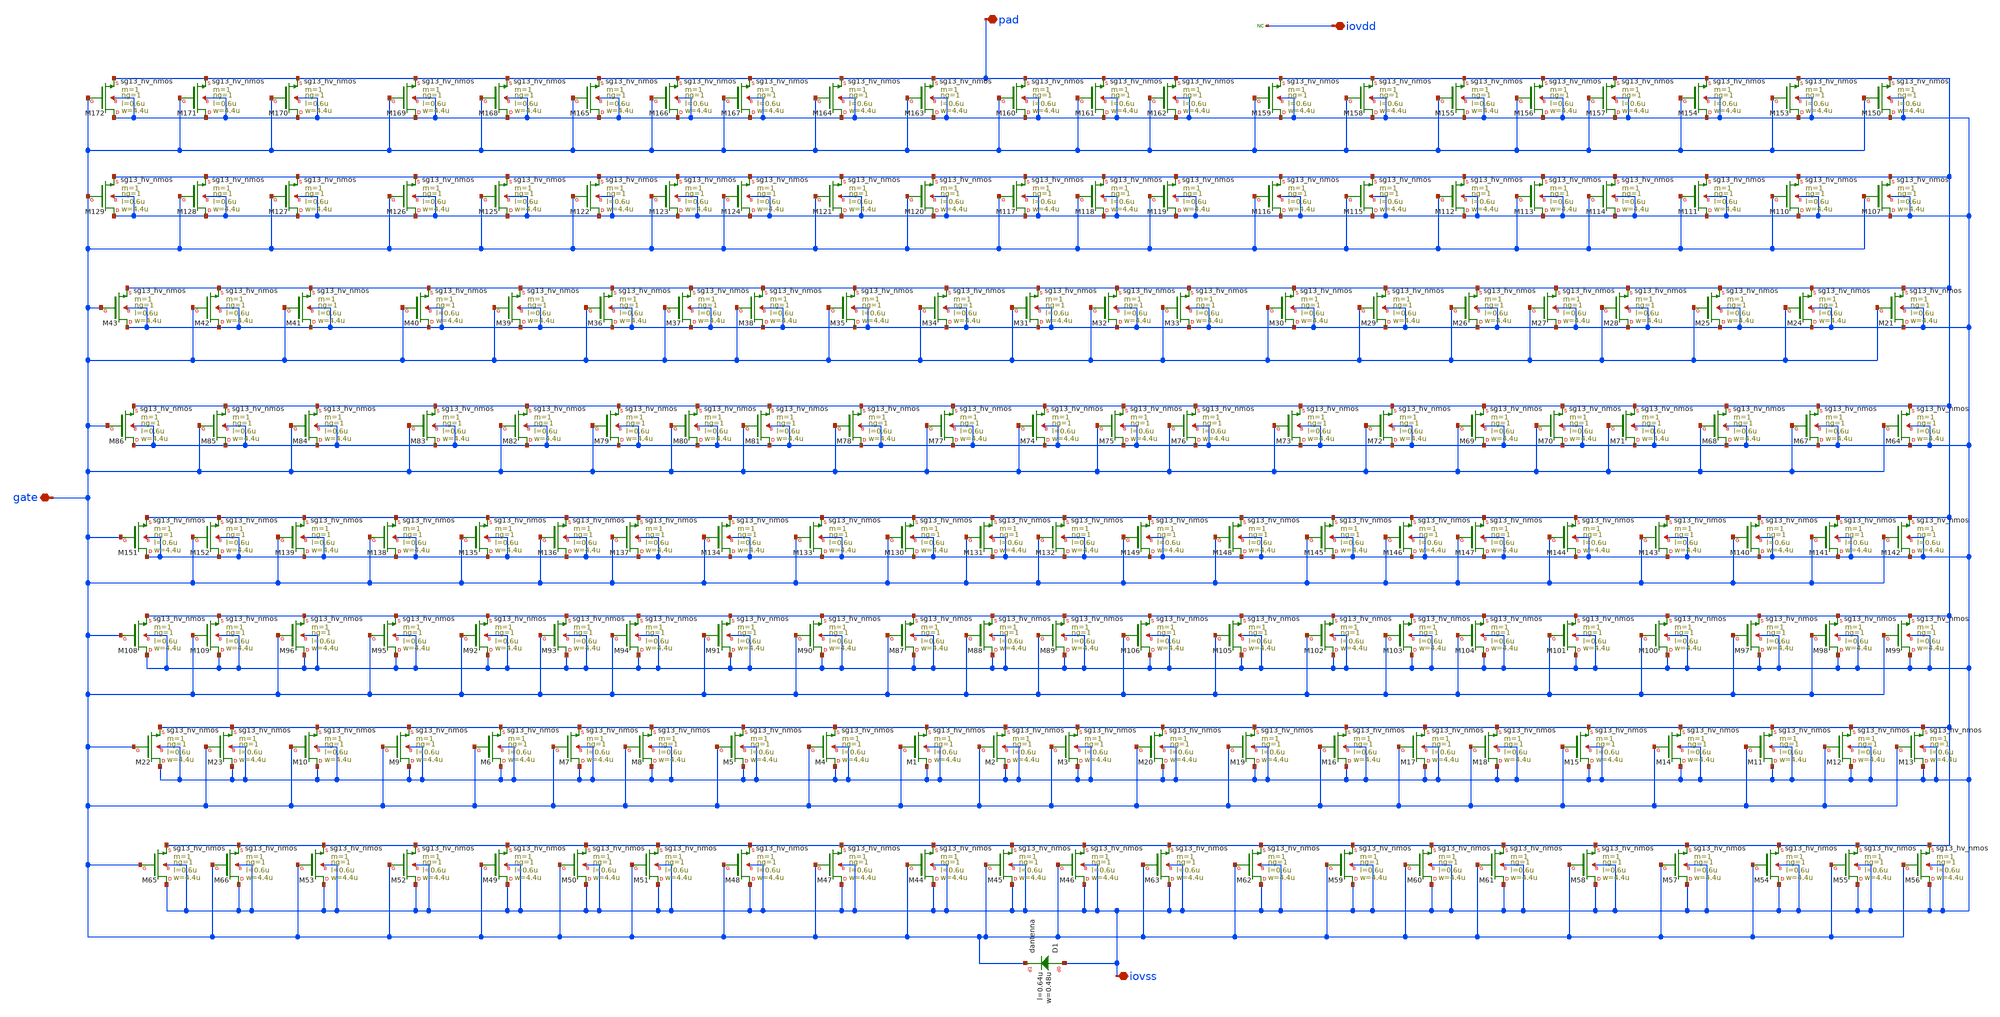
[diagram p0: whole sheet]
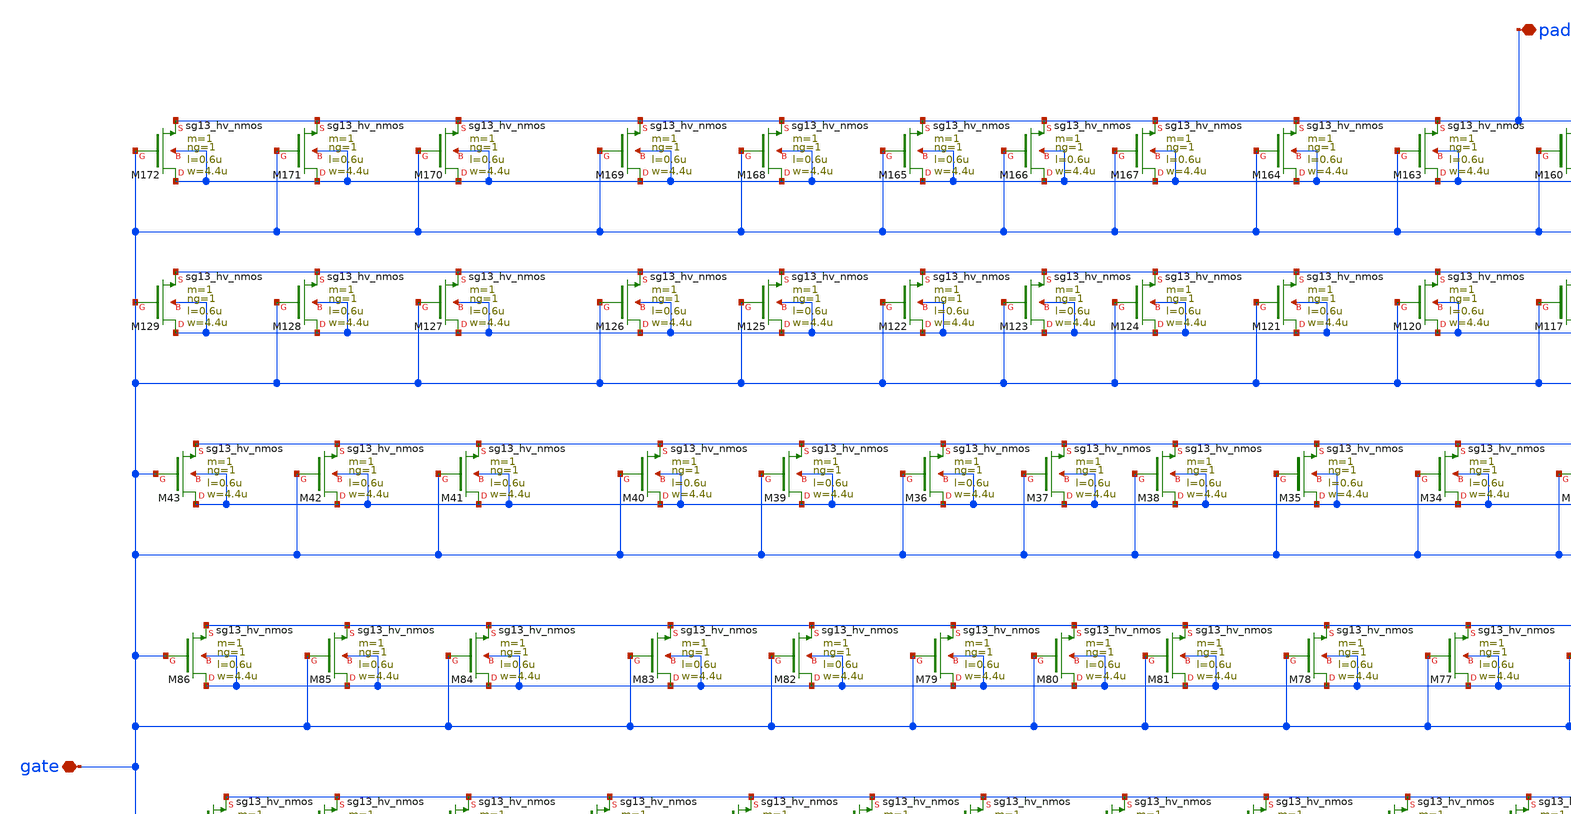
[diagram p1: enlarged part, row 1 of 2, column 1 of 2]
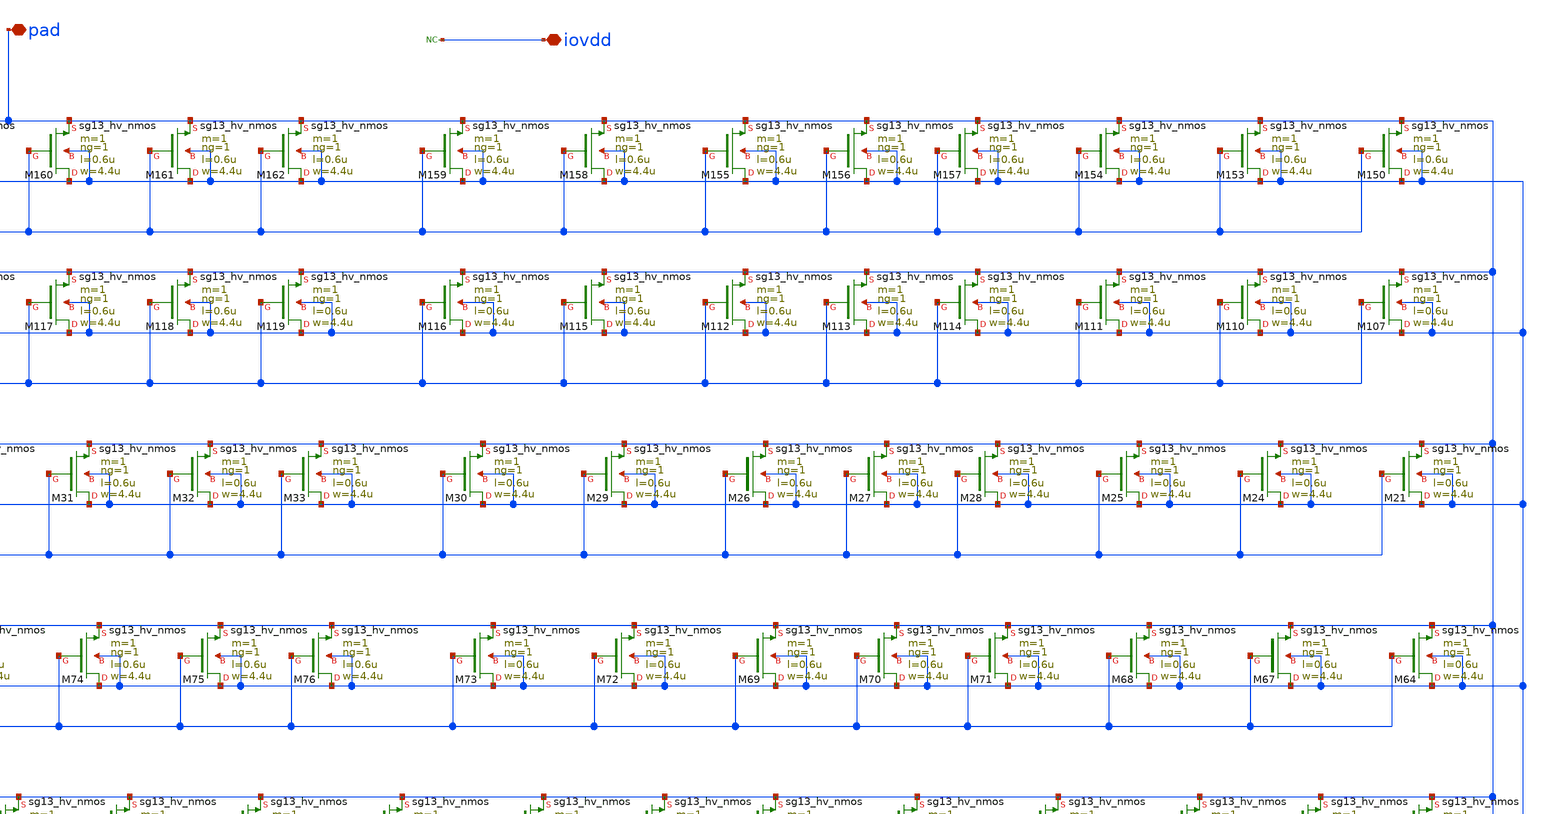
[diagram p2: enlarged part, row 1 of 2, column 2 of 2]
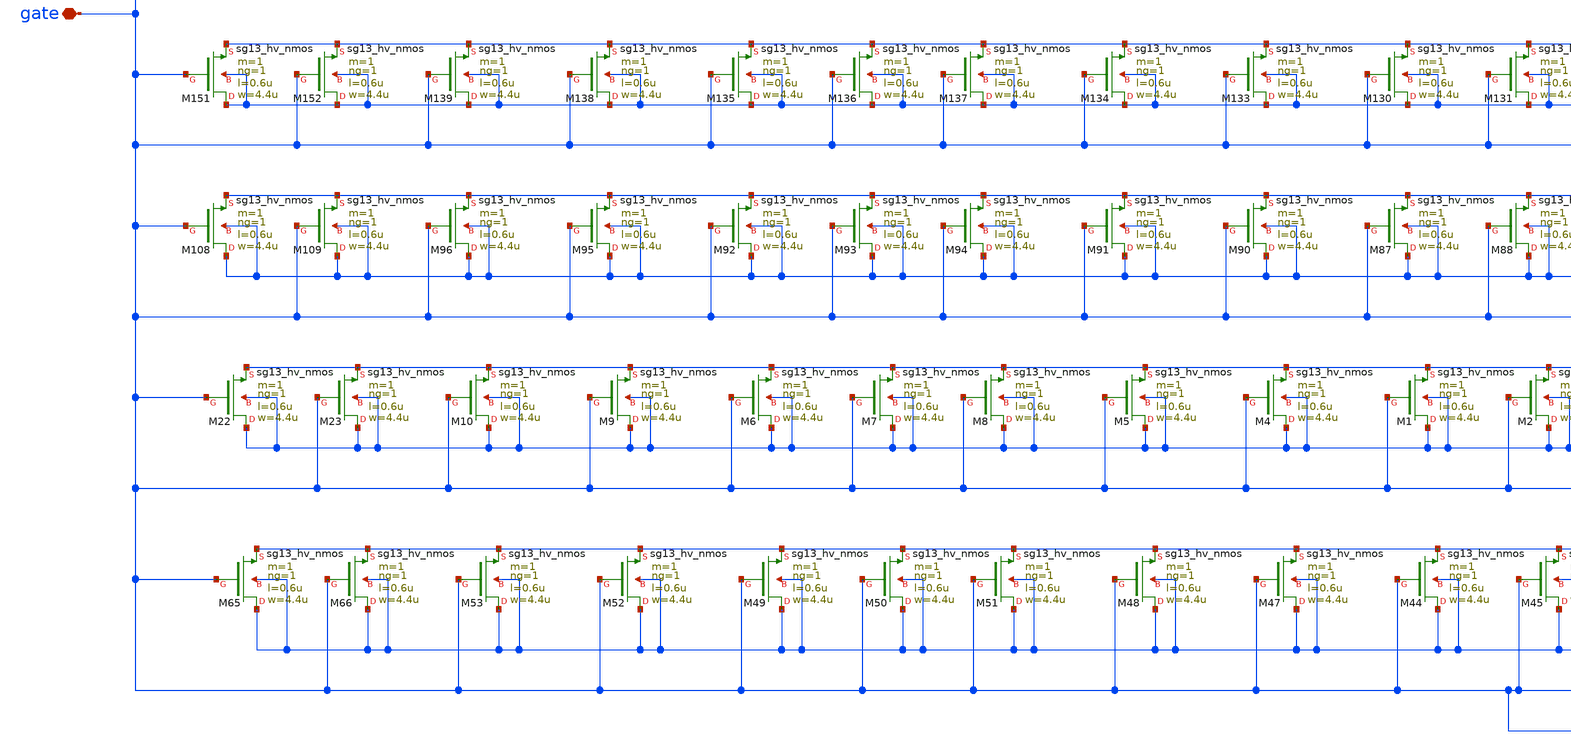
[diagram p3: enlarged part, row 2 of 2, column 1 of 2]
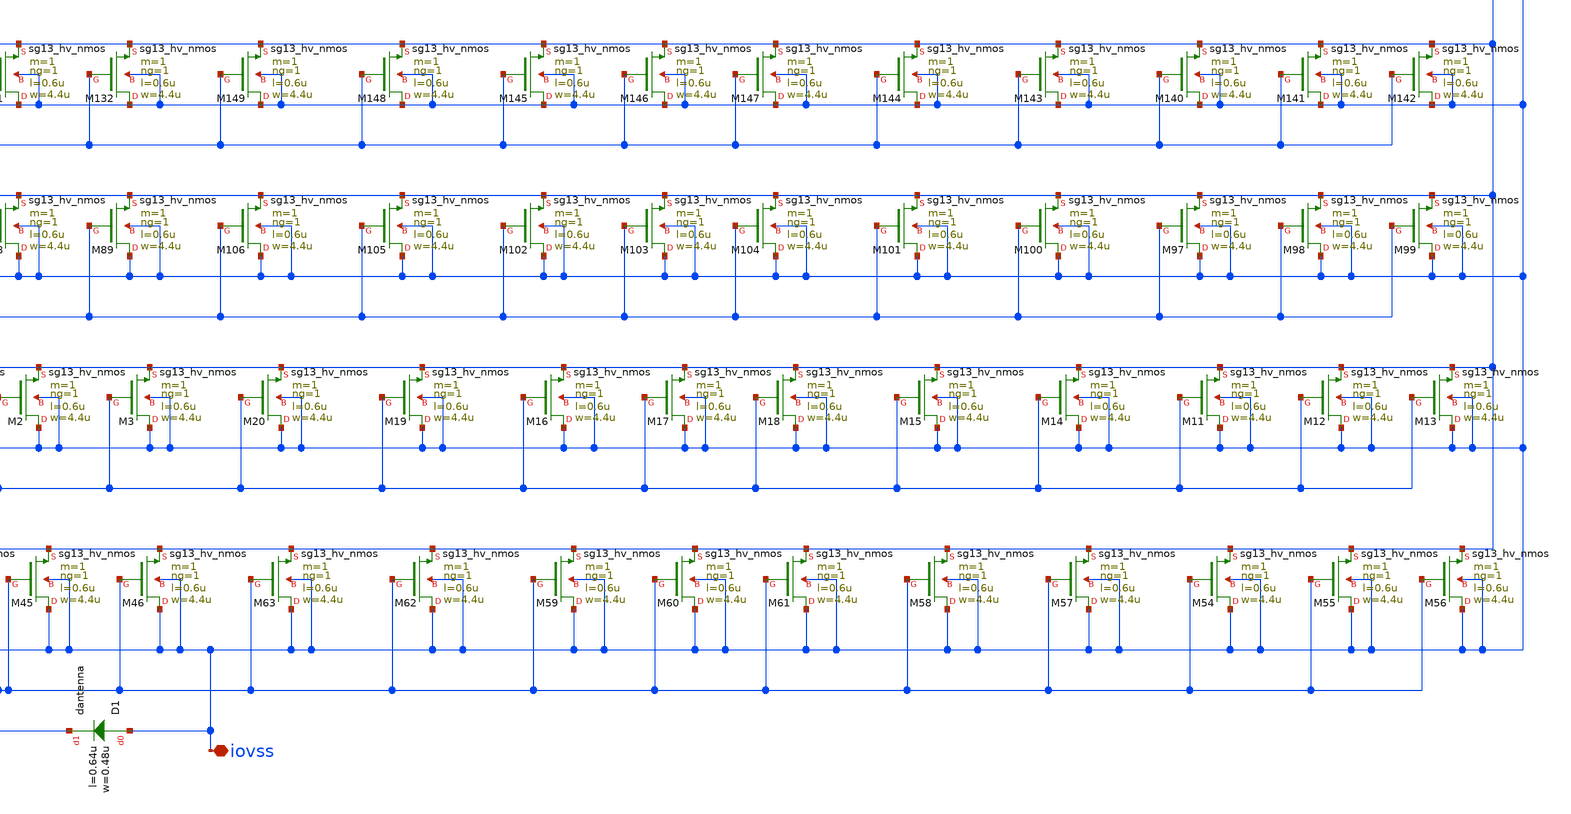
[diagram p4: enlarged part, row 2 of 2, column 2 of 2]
** sch_path: OTA_Telescopic_v3/Schematics_and_Symbols/IOCells/sg13g2_Clamp_N43N43D4R.sch
**.subckt sg13g2_Clamp_N43N43D4R pad iovss gate iovdd
*.iopin pad
*.iopin iovss
*.iopin gate
*.iopin iovdd
XM1 iovss gate pad iovss sg13_hv_nmos w=4.4u l=0.6u ng=1 m=1 mm_ok=1
XM2 iovss gate pad iovss sg13_hv_nmos w=4.4u l=0.6u ng=1 m=1 mm_ok=1
XM3 iovss gate pad iovss sg13_hv_nmos w=4.4u l=0.6u ng=1 m=1 mm_ok=1
XM4 iovss gate pad iovss sg13_hv_nmos w=4.4u l=0.6u ng=1 m=1 mm_ok=1
XM5 iovss gate pad iovss sg13_hv_nmos w=4.4u l=0.6u ng=1 m=1 mm_ok=1
XM6 iovss gate pad iovss sg13_hv_nmos w=4.4u l=0.6u ng=1 m=1 mm_ok=1
XM7 iovss gate pad iovss sg13_hv_nmos w=4.4u l=0.6u ng=1 m=1 mm_ok=1
XM8 iovss gate pad iovss sg13_hv_nmos w=4.4u l=0.6u ng=1 m=1 mm_ok=1
XM9 iovss gate pad iovss sg13_hv_nmos w=4.4u l=0.6u ng=1 m=1 mm_ok=1
XM10 iovss gate pad iovss sg13_hv_nmos w=4.4u l=0.6u ng=1 m=1 mm_ok=1
XM11 iovss gate pad iovss sg13_hv_nmos w=4.4u l=0.6u ng=1 m=1 mm_ok=1
XM12 iovss gate pad iovss sg13_hv_nmos w=4.4u l=0.6u ng=1 m=1 mm_ok=1
XM13 iovss gate pad iovss sg13_hv_nmos w=4.4u l=0.6u ng=1 m=1 mm_ok=1
XM14 iovss gate pad iovss sg13_hv_nmos w=4.4u l=0.6u ng=1 m=1 mm_ok=1
XM15 iovss gate pad iovss sg13_hv_nmos w=4.4u l=0.6u ng=1 m=1 mm_ok=1
XM16 iovss gate pad iovss sg13_hv_nmos w=4.4u l=0.6u ng=1 m=1 mm_ok=1
XM17 iovss gate pad iovss sg13_hv_nmos w=4.4u l=0.6u ng=1 m=1 mm_ok=1
XM18 iovss gate pad iovss sg13_hv_nmos w=4.4u l=0.6u ng=1 m=1 mm_ok=1
XM19 iovss gate pad iovss sg13_hv_nmos w=4.4u l=0.6u ng=1 m=1 mm_ok=1
XM20 iovss gate pad iovss sg13_hv_nmos w=4.4u l=0.6u ng=1 m=1 mm_ok=1
XM21 iovss gate pad iovss sg13_hv_nmos w=4.4u l=0.6u ng=1 m=1 mm_ok=1
XM22 iovss gate pad iovss sg13_hv_nmos w=4.4u l=0.6u ng=1 m=1 mm_ok=1
XM23 iovss gate pad iovss sg13_hv_nmos w=4.4u l=0.6u ng=1 m=1 mm_ok=1
XM24 iovss gate pad iovss sg13_hv_nmos w=4.4u l=0.6u ng=1 m=1 mm_ok=1
XM25 iovss gate pad iovss sg13_hv_nmos w=4.4u l=0.6u ng=1 m=1 mm_ok=1
XM26 iovss gate pad iovss sg13_hv_nmos w=4.4u l=0.6u ng=1 m=1 mm_ok=1
XM27 iovss gate pad iovss sg13_hv_nmos w=4.4u l=0.6u ng=1 m=1 mm_ok=1
XM28 iovss gate pad iovss sg13_hv_nmos w=4.4u l=0.6u ng=1 m=1 mm_ok=1
XM29 iovss gate pad iovss sg13_hv_nmos w=4.4u l=0.6u ng=1 m=1 mm_ok=1
XM30 iovss gate pad iovss sg13_hv_nmos w=4.4u l=0.6u ng=1 m=1 mm_ok=1
XM31 iovss gate pad iovss sg13_hv_nmos w=4.4u l=0.6u ng=1 m=1 mm_ok=1
XM32 iovss gate pad iovss sg13_hv_nmos w=4.4u l=0.6u ng=1 m=1 mm_ok=1
XM33 iovss gate pad iovss sg13_hv_nmos w=4.4u l=0.6u ng=1 m=1 mm_ok=1
XM34 iovss gate pad iovss sg13_hv_nmos w=4.4u l=0.6u ng=1 m=1 mm_ok=1
XM35 iovss gate pad iovss sg13_hv_nmos w=4.4u l=0.6u ng=1 m=1 mm_ok=1
XM36 iovss gate pad iovss sg13_hv_nmos w=4.4u l=0.6u ng=1 m=1 mm_ok=1
XM37 iovss gate pad iovss sg13_hv_nmos w=4.4u l=0.6u ng=1 m=1 mm_ok=1
XM38 iovss gate pad iovss sg13_hv_nmos w=4.4u l=0.6u ng=1 m=1 mm_ok=1
XM39 iovss gate pad iovss sg13_hv_nmos w=4.4u l=0.6u ng=1 m=1 mm_ok=1
XM40 iovss gate pad iovss sg13_hv_nmos w=4.4u l=0.6u ng=1 m=1 mm_ok=1
XM41 iovss gate pad iovss sg13_hv_nmos w=4.4u l=0.6u ng=1 m=1 mm_ok=1
XM42 iovss gate pad iovss sg13_hv_nmos w=4.4u l=0.6u ng=1 m=1 mm_ok=1
XM43 iovss gate pad iovss sg13_hv_nmos w=4.4u l=0.6u ng=1 m=1 mm_ok=1
XM44 iovss gate pad iovss sg13_hv_nmos w=4.4u l=0.6u ng=1 m=1 mm_ok=1
XM45 iovss gate pad iovss sg13_hv_nmos w=4.4u l=0.6u ng=1 m=1 mm_ok=1
XM46 iovss gate pad iovss sg13_hv_nmos w=4.4u l=0.6u ng=1 m=1 mm_ok=1
XM47 iovss gate pad iovss sg13_hv_nmos w=4.4u l=0.6u ng=1 m=1 mm_ok=1
XM48 iovss gate pad iovss sg13_hv_nmos w=4.4u l=0.6u ng=1 m=1 mm_ok=1
XM49 iovss gate pad iovss sg13_hv_nmos w=4.4u l=0.6u ng=1 m=1 mm_ok=1
XM50 iovss gate pad iovss sg13_hv_nmos w=4.4u l=0.6u ng=1 m=1 mm_ok=1
XM51 iovss gate pad iovss sg13_hv_nmos w=4.4u l=0.6u ng=1 m=1 mm_ok=1
XM52 iovss gate pad iovss sg13_hv_nmos w=4.4u l=0.6u ng=1 m=1 mm_ok=1
XM53 iovss gate pad iovss sg13_hv_nmos w=4.4u l=0.6u ng=1 m=1 mm_ok=1
XM54 iovss gate pad iovss sg13_hv_nmos w=4.4u l=0.6u ng=1 m=1 mm_ok=1
XM55 iovss gate pad iovss sg13_hv_nmos w=4.4u l=0.6u ng=1 m=1 mm_ok=1
XM56 iovss gate pad iovss sg13_hv_nmos w=4.4u l=0.6u ng=1 m=1 mm_ok=1
XM57 iovss gate pad iovss sg13_hv_nmos w=4.4u l=0.6u ng=1 m=1 mm_ok=1
XM58 iovss gate pad iovss sg13_hv_nmos w=4.4u l=0.6u ng=1 m=1 mm_ok=1
XM59 iovss gate pad iovss sg13_hv_nmos w=4.4u l=0.6u ng=1 m=1 mm_ok=1
XM60 iovss gate pad iovss sg13_hv_nmos w=4.4u l=0.6u ng=1 m=1 mm_ok=1
XM61 iovss gate pad iovss sg13_hv_nmos w=4.4u l=0.6u ng=1 m=1 mm_ok=1
XM62 iovss gate pad iovss sg13_hv_nmos w=4.4u l=0.6u ng=1 m=1 mm_ok=1
XM63 iovss gate pad iovss sg13_hv_nmos w=4.4u l=0.6u ng=1 m=1 mm_ok=1
XM64 iovss gate pad iovss sg13_hv_nmos w=4.4u l=0.6u ng=1 m=1 mm_ok=1
XM65 iovss gate pad iovss sg13_hv_nmos w=4.4u l=0.6u ng=1 m=1 mm_ok=1
XM66 iovss gate pad iovss sg13_hv_nmos w=4.4u l=0.6u ng=1 m=1 mm_ok=1
XM67 iovss gate pad iovss sg13_hv_nmos w=4.4u l=0.6u ng=1 m=1 mm_ok=1
XM68 iovss gate pad iovss sg13_hv_nmos w=4.4u l=0.6u ng=1 m=1 mm_ok=1
XM69 iovss gate pad iovss sg13_hv_nmos w=4.4u l=0.6u ng=1 m=1 mm_ok=1
XM70 iovss gate pad iovss sg13_hv_nmos w=4.4u l=0.6u ng=1 m=1 mm_ok=1
XM71 iovss gate pad iovss sg13_hv_nmos w=4.4u l=0.6u ng=1 m=1 mm_ok=1
XM72 iovss gate pad iovss sg13_hv_nmos w=4.4u l=0.6u ng=1 m=1 mm_ok=1
XM73 iovss gate pad iovss sg13_hv_nmos w=4.4u l=0.6u ng=1 m=1 mm_ok=1
XM74 iovss gate pad iovss sg13_hv_nmos w=4.4u l=0.6u ng=1 m=1 mm_ok=1
XM75 iovss gate pad iovss sg13_hv_nmos w=4.4u l=0.6u ng=1 m=1 mm_ok=1
XM76 iovss gate pad iovss sg13_hv_nmos w=4.4u l=0.6u ng=1 m=1 mm_ok=1
XM77 iovss gate pad iovss sg13_hv_nmos w=4.4u l=0.6u ng=1 m=1 mm_ok=1
XM78 iovss gate pad iovss sg13_hv_nmos w=4.4u l=0.6u ng=1 m=1 mm_ok=1
XM79 iovss gate pad iovss sg13_hv_nmos w=4.4u l=0.6u ng=1 m=1 mm_ok=1
XM80 iovss gate pad iovss sg13_hv_nmos w=4.4u l=0.6u ng=1 m=1 mm_ok=1
XM81 iovss gate pad iovss sg13_hv_nmos w=4.4u l=0.6u ng=1 m=1 mm_ok=1
XM82 iovss gate pad iovss sg13_hv_nmos w=4.4u l=0.6u ng=1 m=1 mm_ok=1
XM83 iovss gate pad iovss sg13_hv_nmos w=4.4u l=0.6u ng=1 m=1 mm_ok=1
XM84 iovss gate pad iovss sg13_hv_nmos w=4.4u l=0.6u ng=1 m=1 mm_ok=1
XM85 iovss gate pad iovss sg13_hv_nmos w=4.4u l=0.6u ng=1 m=1 mm_ok=1
XM86 iovss gate pad iovss sg13_hv_nmos w=4.4u l=0.6u ng=1 m=1 mm_ok=1
XM87 iovss gate pad iovss sg13_hv_nmos w=4.4u l=0.6u ng=1 m=1 mm_ok=1
XM88 iovss gate pad iovss sg13_hv_nmos w=4.4u l=0.6u ng=1 m=1 mm_ok=1
XM89 iovss gate pad iovss sg13_hv_nmos w=4.4u l=0.6u ng=1 m=1 mm_ok=1
XM90 iovss gate pad iovss sg13_hv_nmos w=4.4u l=0.6u ng=1 m=1 mm_ok=1
XM91 iovss gate pad iovss sg13_hv_nmos w=4.4u l=0.6u ng=1 m=1 mm_ok=1
XM92 iovss gate pad iovss sg13_hv_nmos w=4.4u l=0.6u ng=1 m=1 mm_ok=1
XM93 iovss gate pad iovss sg13_hv_nmos w=4.4u l=0.6u ng=1 m=1 mm_ok=1
XM94 iovss gate pad iovss sg13_hv_nmos w=4.4u l=0.6u ng=1 m=1 mm_ok=1
XM95 iovss gate pad iovss sg13_hv_nmos w=4.4u l=0.6u ng=1 m=1 mm_ok=1
XM96 iovss gate pad iovss sg13_hv_nmos w=4.4u l=0.6u ng=1 m=1 mm_ok=1
XM97 iovss gate pad iovss sg13_hv_nmos w=4.4u l=0.6u ng=1 m=1 mm_ok=1
XM98 iovss gate pad iovss sg13_hv_nmos w=4.4u l=0.6u ng=1 m=1 mm_ok=1
XM99 iovss gate pad iovss sg13_hv_nmos w=4.4u l=0.6u ng=1 m=1 mm_ok=1
XM100 iovss gate pad iovss sg13_hv_nmos w=4.4u l=0.6u ng=1 m=1 mm_ok=1
XM101 iovss gate pad iovss sg13_hv_nmos w=4.4u l=0.6u ng=1 m=1 mm_ok=1
XM102 iovss gate pad iovss sg13_hv_nmos w=4.4u l=0.6u ng=1 m=1 mm_ok=1
XM103 iovss gate pad iovss sg13_hv_nmos w=4.4u l=0.6u ng=1 m=1 mm_ok=1
XM104 iovss gate pad iovss sg13_hv_nmos w=4.4u l=0.6u ng=1 m=1 mm_ok=1
XM105 iovss gate pad iovss sg13_hv_nmos w=4.4u l=0.6u ng=1 m=1 mm_ok=1
XM106 iovss gate pad iovss sg13_hv_nmos w=4.4u l=0.6u ng=1 m=1 mm_ok=1
XM107 iovss gate pad iovss sg13_hv_nmos w=4.4u l=0.6u ng=1 m=1 mm_ok=1
XM108 iovss gate pad iovss sg13_hv_nmos w=4.4u l=0.6u ng=1 m=1 mm_ok=1
XM109 iovss gate pad iovss sg13_hv_nmos w=4.4u l=0.6u ng=1 m=1 mm_ok=1
XM110 iovss gate pad iovss sg13_hv_nmos w=4.4u l=0.6u ng=1 m=1 mm_ok=1
XM111 iovss gate pad iovss sg13_hv_nmos w=4.4u l=0.6u ng=1 m=1 mm_ok=1
XM112 iovss gate pad iovss sg13_hv_nmos w=4.4u l=0.6u ng=1 m=1 mm_ok=1
XM113 iovss gate pad iovss sg13_hv_nmos w=4.4u l=0.6u ng=1 m=1 mm_ok=1
XM114 iovss gate pad iovss sg13_hv_nmos w=4.4u l=0.6u ng=1 m=1 mm_ok=1
XM115 iovss gate pad iovss sg13_hv_nmos w=4.4u l=0.6u ng=1 m=1 mm_ok=1
XM116 iovss gate pad iovss sg13_hv_nmos w=4.4u l=0.6u ng=1 m=1 mm_ok=1
XM117 iovss gate pad iovss sg13_hv_nmos w=4.4u l=0.6u ng=1 m=1 mm_ok=1
XM118 iovss gate pad iovss sg13_hv_nmos w=4.4u l=0.6u ng=1 m=1 mm_ok=1
XM119 iovss gate pad iovss sg13_hv_nmos w=4.4u l=0.6u ng=1 m=1 mm_ok=1
XM120 iovss gate pad iovss sg13_hv_nmos w=4.4u l=0.6u ng=1 m=1 mm_ok=1
XM121 iovss gate pad iovss sg13_hv_nmos w=4.4u l=0.6u ng=1 m=1 mm_ok=1
XM122 iovss gate pad iovss sg13_hv_nmos w=4.4u l=0.6u ng=1 m=1 mm_ok=1
XM123 iovss gate pad iovss sg13_hv_nmos w=4.4u l=0.6u ng=1 m=1 mm_ok=1
XM124 iovss gate pad iovss sg13_hv_nmos w=4.4u l=0.6u ng=1 m=1 mm_ok=1
XM125 iovss gate pad iovss sg13_hv_nmos w=4.4u l=0.6u ng=1 m=1 mm_ok=1
XM126 iovss gate pad iovss sg13_hv_nmos w=4.4u l=0.6u ng=1 m=1 mm_ok=1
XM127 iovss gate pad iovss sg13_hv_nmos w=4.4u l=0.6u ng=1 m=1 mm_ok=1
XM128 iovss gate pad iovss sg13_hv_nmos w=4.4u l=0.6u ng=1 m=1 mm_ok=1
XM129 iovss gate pad iovss sg13_hv_nmos w=4.4u l=0.6u ng=1 m=1 mm_ok=1
XM130 iovss gate pad iovss sg13_hv_nmos w=4.4u l=0.6u ng=1 m=1 mm_ok=1
XM131 iovss gate pad iovss sg13_hv_nmos w=4.4u l=0.6u ng=1 m=1 mm_ok=1
XM132 iovss gate pad iovss sg13_hv_nmos w=4.4u l=0.6u ng=1 m=1 mm_ok=1
XM133 iovss gate pad iovss sg13_hv_nmos w=4.4u l=0.6u ng=1 m=1 mm_ok=1
XM134 iovss gate pad iovss sg13_hv_nmos w=4.4u l=0.6u ng=1 m=1 mm_ok=1
XM135 iovss gate pad iovss sg13_hv_nmos w=4.4u l=0.6u ng=1 m=1 mm_ok=1
XM136 iovss gate pad iovss sg13_hv_nmos w=4.4u l=0.6u ng=1 m=1 mm_ok=1
XM137 iovss gate pad iovss sg13_hv_nmos w=4.4u l=0.6u ng=1 m=1 mm_ok=1
XM138 iovss gate pad iovss sg13_hv_nmos w=4.4u l=0.6u ng=1 m=1 mm_ok=1
XM139 iovss gate pad iovss sg13_hv_nmos w=4.4u l=0.6u ng=1 m=1 mm_ok=1
XM140 iovss gate pad iovss sg13_hv_nmos w=4.4u l=0.6u ng=1 m=1 mm_ok=1
XM141 iovss gate pad iovss sg13_hv_nmos w=4.4u l=0.6u ng=1 m=1 mm_ok=1
XM142 iovss gate pad iovss sg13_hv_nmos w=4.4u l=0.6u ng=1 m=1 mm_ok=1
XM143 iovss gate pad iovss sg13_hv_nmos w=4.4u l=0.6u ng=1 m=1 mm_ok=1
XM144 iovss gate pad iovss sg13_hv_nmos w=4.4u l=0.6u ng=1 m=1 mm_ok=1
XM145 iovss gate pad iovss sg13_hv_nmos w=4.4u l=0.6u ng=1 m=1 mm_ok=1
XM146 iovss gate pad iovss sg13_hv_nmos w=4.4u l=0.6u ng=1 m=1 mm_ok=1
XM147 iovss gate pad iovss sg13_hv_nmos w=4.4u l=0.6u ng=1 m=1 mm_ok=1
XM148 iovss gate pad iovss sg13_hv_nmos w=4.4u l=0.6u ng=1 m=1 mm_ok=1
XM149 iovss gate pad iovss sg13_hv_nmos w=4.4u l=0.6u ng=1 m=1 mm_ok=1
XM150 iovss gate pad iovss sg13_hv_nmos w=4.4u l=0.6u ng=1 m=1 mm_ok=1
XM151 iovss gate pad iovss sg13_hv_nmos w=4.4u l=0.6u ng=1 m=1 mm_ok=1
XM152 iovss gate pad iovss sg13_hv_nmos w=4.4u l=0.6u ng=1 m=1 mm_ok=1
XM153 iovss gate pad iovss sg13_hv_nmos w=4.4u l=0.6u ng=1 m=1 mm_ok=1
XM154 iovss gate pad iovss sg13_hv_nmos w=4.4u l=0.6u ng=1 m=1 mm_ok=1
XM155 iovss gate pad iovss sg13_hv_nmos w=4.4u l=0.6u ng=1 m=1 mm_ok=1
XM156 iovss gate pad iovss sg13_hv_nmos w=4.4u l=0.6u ng=1 m=1 mm_ok=1
XM157 iovss gate pad iovss sg13_hv_nmos w=4.4u l=0.6u ng=1 m=1 mm_ok=1
XM158 iovss gate pad iovss sg13_hv_nmos w=4.4u l=0.6u ng=1 m=1 mm_ok=1
XM159 iovss gate pad iovss sg13_hv_nmos w=4.4u l=0.6u ng=1 m=1 mm_ok=1
XM160 iovss gate pad iovss sg13_hv_nmos w=4.4u l=0.6u ng=1 m=1 mm_ok=1
XM161 iovss gate pad iovss sg13_hv_nmos w=4.4u l=0.6u ng=1 m=1 mm_ok=1
XM162 iovss gate pad iovss sg13_hv_nmos w=4.4u l=0.6u ng=1 m=1 mm_ok=1
XM163 iovss gate pad iovss sg13_hv_nmos w=4.4u l=0.6u ng=1 m=1 mm_ok=1
XM164 iovss gate pad iovss sg13_hv_nmos w=4.4u l=0.6u ng=1 m=1 mm_ok=1
XM165 iovss gate pad iovss sg13_hv_nmos w=4.4u l=0.6u ng=1 m=1 mm_ok=1
XM166 iovss gate pad iovss sg13_hv_nmos w=4.4u l=0.6u ng=1 m=1 mm_ok=1
XM167 iovss gate pad iovss sg13_hv_nmos w=4.4u l=0.6u ng=1 m=1 mm_ok=1
XM168 iovss gate pad iovss sg13_hv_nmos w=4.4u l=0.6u ng=1 m=1 mm_ok=1
XM169 iovss gate pad iovss sg13_hv_nmos w=4.4u l=0.6u ng=1 m=1 mm_ok=1
XM170 iovss gate pad iovss sg13_hv_nmos w=4.4u l=0.6u ng=1 m=1 mm_ok=1
XM171 iovss gate pad iovss sg13_hv_nmos w=4.4u l=0.6u ng=1 m=1 mm_ok=1
XM172 iovss gate pad iovss sg13_hv_nmos w=4.4u l=0.6u ng=1 m=1 mm_ok=1
XD1 iovss gate dantenna l=0.64u w=0.48u
* noconn iovdd
**.ends
.end
